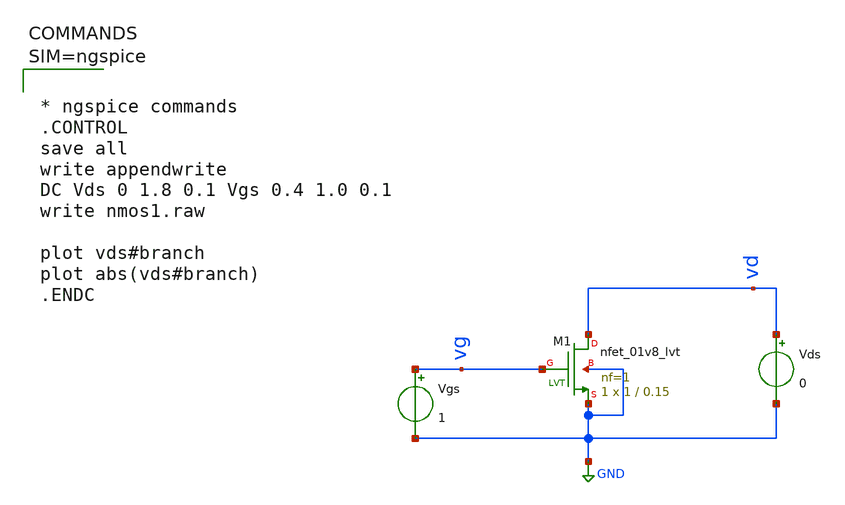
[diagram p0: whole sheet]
** sch_path: work/xschem/nmos1.sch
**.subckt nmos1
XM1 vd vg GND GND sky130_fd_pr__nfet_01v8_lvt L=0.15 W=1 nf=1 ad='int((1 + 1)/2) * 1 / 1 * 0.29' as='int((1 + 2)/2) * 1 / 1 * 0.29'
+ pd='2*int((1 + 1)/2) * (1 / 1 + 0.29)' ps='2*int((1 + 2)/2) * (1 / 1 + 0.29)' nrd='0.29 / 1 ' nrs='0.29 / 1 '
+ sa=0 sb=0 sd=0 mult=1 m=1
Vgs vg GND 1
Vds vd GND 0
**** begin user architecture code



* ngspice commands
.CONTROL
save all
write appendwrite
DC Vds 0 1.8 0.1 Vgs 0.4 1.0 0.1
write nmos1.raw

plot vds#branch
plot abs(vds#branch)
.ENDC




** opencircuitdesign pdks install
.lib $::SKYWATER_MODELS/sky130.lib.spice tt

**** end user architecture code
**.ends
.GLOBAL GND
.end
